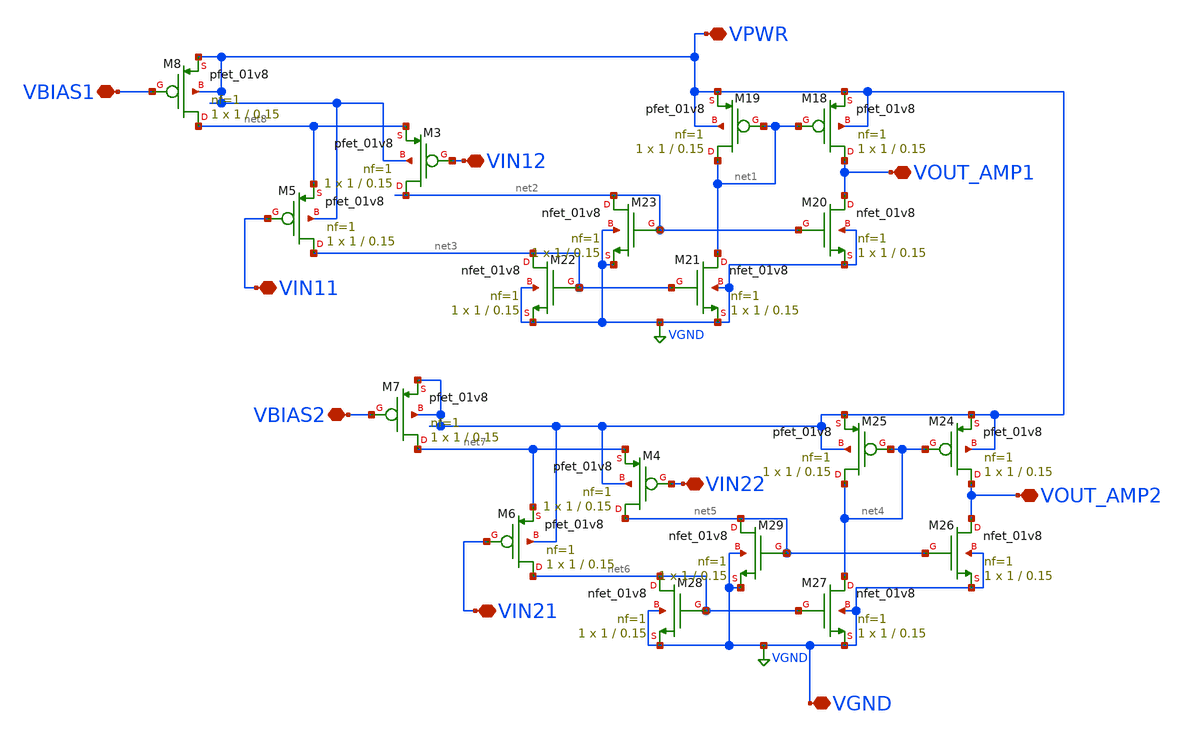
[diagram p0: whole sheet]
** sch_path: libs.ref/sky130_hilas_sc/xschem/sky130_hilas_TA2SignalBiasCell.sch
**.subckt sky130_hilas_TA2SignalBiasCell VPWR VOUT_AMP1 VOUT_AMP2 VIN21 VIN22 VIN11 VIN12 VBIAS1
*+ VBIAS2 VGND
*.iopin VPWR
*.iopin VOUT_AMP1
*.iopin VOUT_AMP2
*.iopin VIN21
*.iopin VIN22
*.iopin VIN11
*.iopin VIN12
*.iopin VBIAS1
*.iopin VBIAS2
*.iopin VGND
XM18 VOUT_AMP1 net1 VPWR VPWR sky130_fd_pr__pfet_01v8 L=0.15 W=1 nf=1 ad='int((nf+1)/2) * W/nf * 0.29'
+ as='int((nf+2)/2) * W/nf * 0.29' pd='2*int((nf+1)/2) * (W/nf + 0.29)' ps='2*int((nf+2)/2) * (W/nf + 0.29)'
+ nrd='0.29 / W' nrs='0.29 / W' sa=0 sb=0 sd=0 mult=1 m=1
XM19 net1 net1 VPWR VPWR sky130_fd_pr__pfet_01v8 L=0.15 W=1 nf=1 ad='int((nf+1)/2) * W/nf * 0.29' as='int((nf+2)/2) * W/nf * 0.29'
+ pd='2*int((nf+1)/2) * (W/nf + 0.29)' ps='2*int((nf+2)/2) * (W/nf + 0.29)' nrd='0.29 / W' nrs='0.29 / W'
+ sa=0 sb=0 sd=0 mult=1 m=1
XM20 VOUT_AMP1 net2 VGND VGND sky130_fd_pr__nfet_01v8 L=0.15 W=1 nf=1 ad='int((nf+1)/2) * W/nf * 0.29'
+ as='int((nf+2)/2) * W/nf * 0.29' pd='2*int((nf+1)/2) * (W/nf + 0.29)' ps='2*int((nf+2)/2) * (W/nf + 0.29)'
+ nrd='0.29 / W' nrs='0.29 / W' sa=0 sb=0 sd=0 mult=1 m=1
XM21 net1 net3 VGND VGND sky130_fd_pr__nfet_01v8 L=0.15 W=1 nf=1 ad='int((nf+1)/2) * W/nf * 0.29' as='int((nf+2)/2) * W/nf * 0.29'
+ pd='2*int((nf+1)/2) * (W/nf + 0.29)' ps='2*int((nf+2)/2) * (W/nf + 0.29)' nrd='0.29 / W' nrs='0.29 / W'
+ sa=0 sb=0 sd=0 mult=1 m=1
XM22 net3 net3 VGND VGND sky130_fd_pr__nfet_01v8 L=0.15 W=1 nf=1 ad='int((nf+1)/2) * W/nf * 0.29' as='int((nf+2)/2) * W/nf * 0.29'
+ pd='2*int((nf+1)/2) * (W/nf + 0.29)' ps='2*int((nf+2)/2) * (W/nf + 0.29)' nrd='0.29 / W' nrs='0.29 / W'
+ sa=0 sb=0 sd=0 mult=1 m=1
XM23 net2 net2 VGND VGND sky130_fd_pr__nfet_01v8 L=0.15 W=1 nf=1 ad='int((nf+1)/2) * W/nf * 0.29' as='int((nf+2)/2) * W/nf * 0.29'
+ pd='2*int((nf+1)/2) * (W/nf + 0.29)' ps='2*int((nf+2)/2) * (W/nf + 0.29)' nrd='0.29 / W' nrs='0.29 / W'
+ sa=0 sb=0 sd=0 mult=1 m=1
XM24 VOUT_AMP2 net4 VPWR VPWR sky130_fd_pr__pfet_01v8 L=0.15 W=1 nf=1 ad='int((nf+1)/2) * W/nf * 0.29'
+ as='int((nf+2)/2) * W/nf * 0.29' pd='2*int((nf+1)/2) * (W/nf + 0.29)' ps='2*int((nf+2)/2) * (W/nf + 0.29)'
+ nrd='0.29 / W' nrs='0.29 / W' sa=0 sb=0 sd=0 mult=1 m=1
XM25 net4 net4 VPWR VPWR sky130_fd_pr__pfet_01v8 L=0.15 W=1 nf=1 ad='int((nf+1)/2) * W/nf * 0.29' as='int((nf+2)/2) * W/nf * 0.29'
+ pd='2*int((nf+1)/2) * (W/nf + 0.29)' ps='2*int((nf+2)/2) * (W/nf + 0.29)' nrd='0.29 / W' nrs='0.29 / W'
+ sa=0 sb=0 sd=0 mult=1 m=1
XM26 VOUT_AMP2 net5 VGND VGND sky130_fd_pr__nfet_01v8 L=0.15 W=1 nf=1 ad='int((nf+1)/2) * W/nf * 0.29'
+ as='int((nf+2)/2) * W/nf * 0.29' pd='2*int((nf+1)/2) * (W/nf + 0.29)' ps='2*int((nf+2)/2) * (W/nf + 0.29)'
+ nrd='0.29 / W' nrs='0.29 / W' sa=0 sb=0 sd=0 mult=1 m=1
XM27 net4 net6 VGND VGND sky130_fd_pr__nfet_01v8 L=0.15 W=1 nf=1 ad='int((nf+1)/2) * W/nf * 0.29' as='int((nf+2)/2) * W/nf * 0.29'
+ pd='2*int((nf+1)/2) * (W/nf + 0.29)' ps='2*int((nf+2)/2) * (W/nf + 0.29)' nrd='0.29 / W' nrs='0.29 / W'
+ sa=0 sb=0 sd=0 mult=1 m=1
XM28 net6 net6 VGND VGND sky130_fd_pr__nfet_01v8 L=0.15 W=1 nf=1 ad='int((nf+1)/2) * W/nf * 0.29' as='int((nf+2)/2) * W/nf * 0.29'
+ pd='2*int((nf+1)/2) * (W/nf + 0.29)' ps='2*int((nf+2)/2) * (W/nf + 0.29)' nrd='0.29 / W' nrs='0.29 / W'
+ sa=0 sb=0 sd=0 mult=1 m=1
XM29 net5 net5 VGND VGND sky130_fd_pr__nfet_01v8 L=0.15 W=1 nf=1 ad='int((nf+1)/2) * W/nf * 0.29' as='int((nf+2)/2) * W/nf * 0.29'
+ pd='2*int((nf+1)/2) * (W/nf + 0.29)' ps='2*int((nf+2)/2) * (W/nf + 0.29)' nrd='0.29 / W' nrs='0.29 / W'
+ sa=0 sb=0 sd=0 mult=1 m=1
XM3 net2 VIN12 net8 VPWR sky130_fd_pr__pfet_01v8 L=0.15 W=1 nf=1 ad='int((nf+1)/2) * W/nf * 0.29' as='int((nf+2)/2) * W/nf * 0.29'
+ pd='2*int((nf+1)/2) * (W/nf + 0.29)' ps='2*int((nf+2)/2) * (W/nf + 0.29)' nrd='0.29 / W' nrs='0.29 / W'
+ sa=0 sb=0 sd=0 mult=1 m=1
XM4 net5 VIN22 net7 VPWR sky130_fd_pr__pfet_01v8 L=0.15 W=1 nf=1 ad='int((nf+1)/2) * W/nf * 0.29' as='int((nf+2)/2) * W/nf * 0.29'
+ pd='2*int((nf+1)/2) * (W/nf + 0.29)' ps='2*int((nf+2)/2) * (W/nf + 0.29)' nrd='0.29 / W' nrs='0.29 / W'
+ sa=0 sb=0 sd=0 mult=1 m=1
XM5 net3 VIN11 net8 VPWR sky130_fd_pr__pfet_01v8 L=0.15 W=1 nf=1 ad='int((nf+1)/2) * W/nf * 0.29' as='int((nf+2)/2) * W/nf * 0.29'
+ pd='2*int((nf+1)/2) * (W/nf + 0.29)' ps='2*int((nf+2)/2) * (W/nf + 0.29)' nrd='0.29 / W' nrs='0.29 / W'
+ sa=0 sb=0 sd=0 mult=1 m=1
XM6 net6 VIN21 net7 VPWR sky130_fd_pr__pfet_01v8 L=0.15 W=1 nf=1 ad='int((nf+1)/2) * W/nf * 0.29' as='int((nf+2)/2) * W/nf * 0.29'
+ pd='2*int((nf+1)/2) * (W/nf + 0.29)' ps='2*int((nf+2)/2) * (W/nf + 0.29)' nrd='0.29 / W' nrs='0.29 / W'
+ sa=0 sb=0 sd=0 mult=1 m=1
XM7 net7 VBIAS2 VPWR VPWR sky130_fd_pr__pfet_01v8 L=0.15 W=1 nf=1 ad='int((nf+1)/2) * W/nf * 0.29' as='int((nf+2)/2) * W/nf * 0.29'
+ pd='2*int((nf+1)/2) * (W/nf + 0.29)' ps='2*int((nf+2)/2) * (W/nf + 0.29)' nrd='0.29 / W' nrs='0.29 / W'
+ sa=0 sb=0 sd=0 mult=1 m=1
XM8 net8 VBIAS1 VPWR VPWR sky130_fd_pr__pfet_01v8 L=0.15 W=1 nf=1 ad='int((nf+1)/2) * W/nf * 0.29' as='int((nf+2)/2) * W/nf * 0.29'
+ pd='2*int((nf+1)/2) * (W/nf + 0.29)' ps='2*int((nf+2)/2) * (W/nf + 0.29)' nrd='0.29 / W' nrs='0.29 / W'
+ sa=0 sb=0 sd=0 mult=1 m=1
**.ends
.GLOBAL VGND
.end
